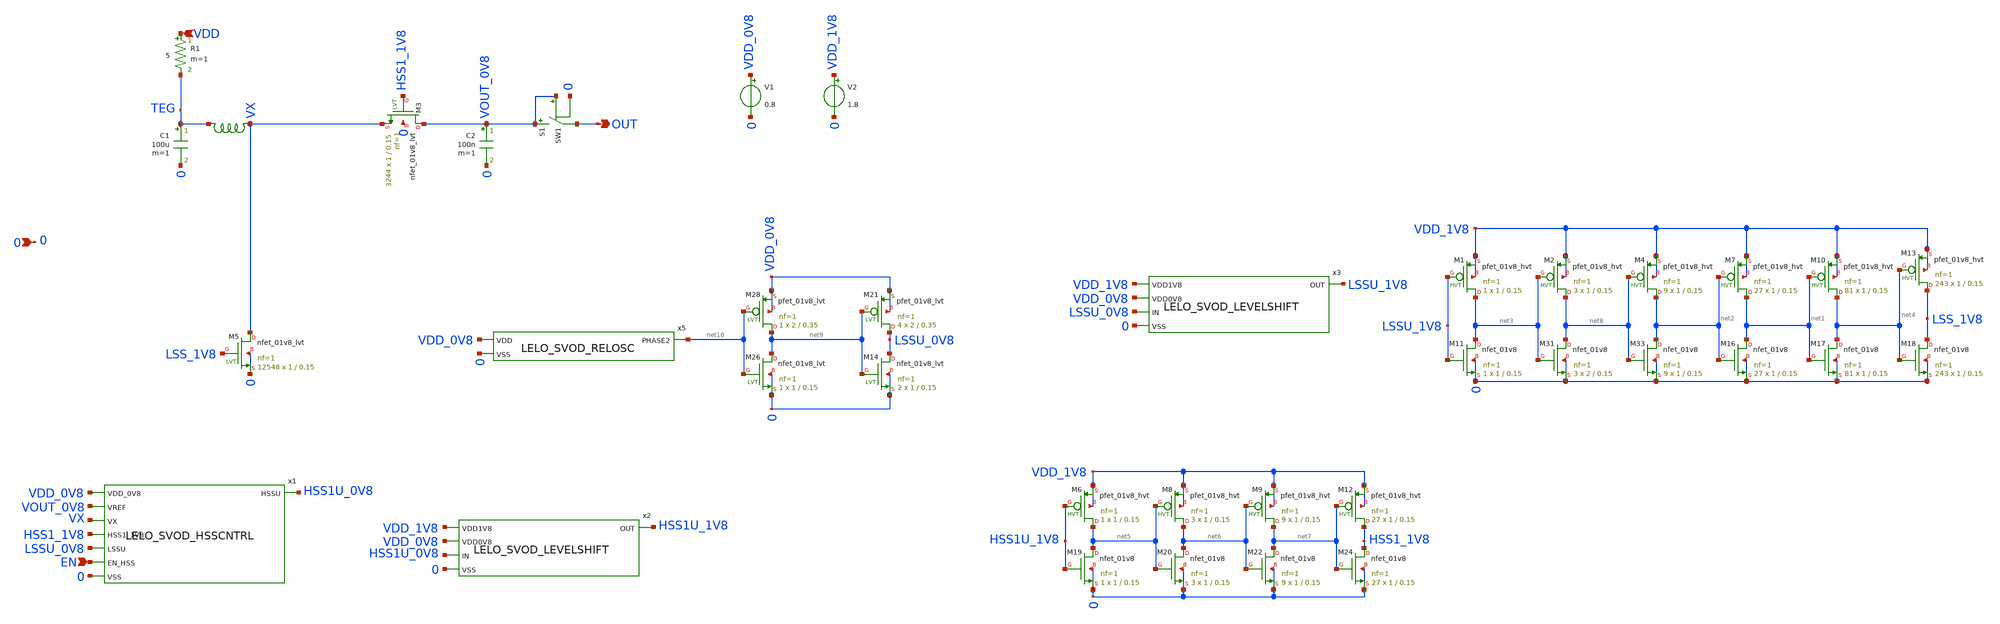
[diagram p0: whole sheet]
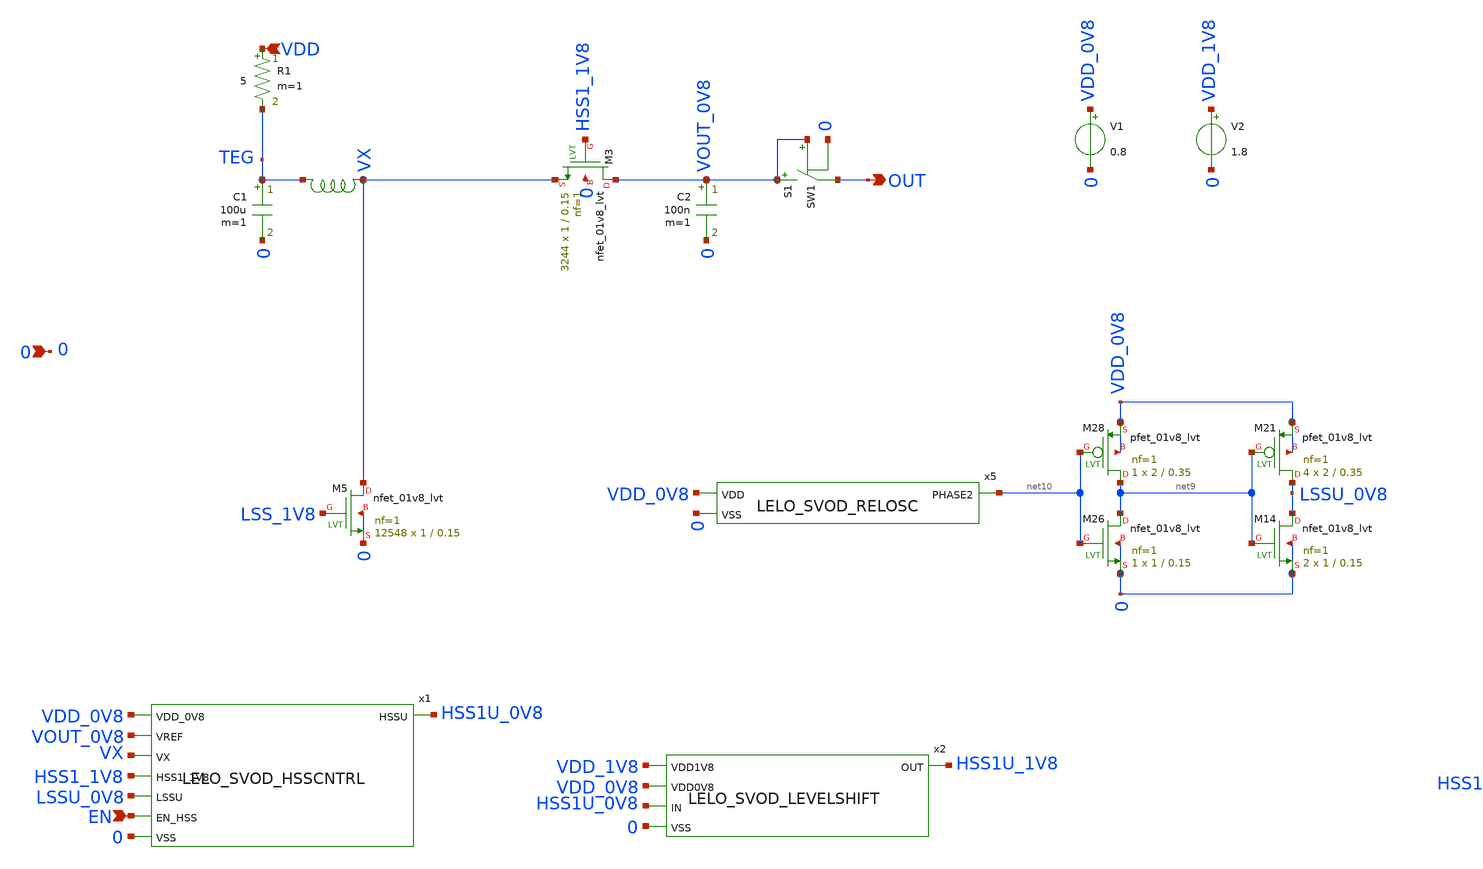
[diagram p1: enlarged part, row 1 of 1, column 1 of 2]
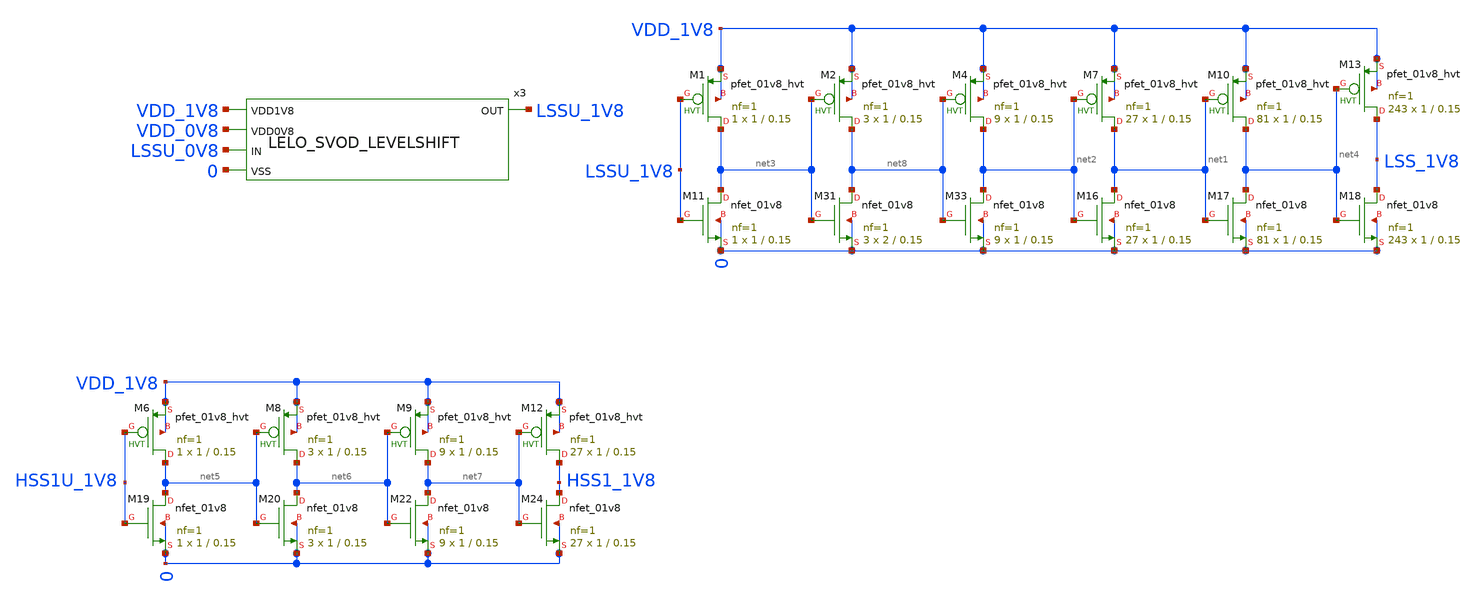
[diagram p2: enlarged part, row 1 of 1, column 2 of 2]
** sch_path: design/LELO_SVOD_SKY130A/LELO_SVOD_0V8_BOOST.sch
**.subckt LELO_SVOD_0V8_BOOST VDD 0 OUT EN
*.ipin VDD
*.ipin 0
*.opin OUT
*.ipin EN
R1 VDD TEG 5 m=1
C1 TEG 0 100u m=1
XM5 VX LSS_1V8 0 0 sky130_fd_pr__nfet_01v8_lvt L=0.15 W=1 nf=1 ad='int((1 + 1)/2) * 1 / 1 * 0.29' as='int((1 + 2)/2) * 1 / 1 * 0.29'
+ pd='2*int((1 + 1)/2) * (1 / 1 + 0.29)' ps='2*int((1 + 2)/2) * (1 / 1 + 0.29)' nrd='0.29 / 1 ' nrs='0.29 / 1 '
+ sa=0 sb=0 sd=0 mult=12548 m=12548
C2 VOUT_0V8 0 100n m=1
XM11 net3 LSSU_1V8 0 0 sky130_fd_pr__nfet_01v8 L=0.15 W=1 nf=1 ad='int((1 + 1)/2) * 1 / 1 * 0.29' as='int((1 + 2)/2) * 1 / 1 * 0.29'
+ pd='2*int((1 + 1)/2) * (1 / 1 + 0.29)' ps='2*int((1 + 2)/2) * (1 / 1 + 0.29)' nrd='0.29 / 1 ' nrs='0.29 / 1 '
+ sa=0 sb=0 sd=0 mult=1 m=1
XM16 net1 net2 0 0 sky130_fd_pr__nfet_01v8 L=0.15 W=1 nf=1 ad='int((1 + 1)/2) * 1 / 1 * 0.29' as='int((1 + 2)/2) * 1 / 1 * 0.29'
+ pd='2*int((1 + 1)/2) * (1 / 1 + 0.29)' ps='2*int((1 + 2)/2) * (1 / 1 + 0.29)' nrd='0.29 / 1 ' nrs='0.29 / 1 '
+ sa=0 sb=0 sd=0 mult=27 m=27
XM17 net4 net1 0 0 sky130_fd_pr__nfet_01v8 L=0.15 W=1 nf=1 ad='int((1 + 1)/2) * 1 / 1 * 0.29' as='int((1 + 2)/2) * 1 / 1 * 0.29'
+ pd='2*int((1 + 1)/2) * (1 / 1 + 0.29)' ps='2*int((1 + 2)/2) * (1 / 1 + 0.29)' nrd='0.29 / 1 ' nrs='0.29 / 1 '
+ sa=0 sb=0 sd=0 mult=81 m=81
XM18 LSS_1V8 net4 0 0 sky130_fd_pr__nfet_01v8 L=0.15 W=1 nf=1 ad='int((1 + 1)/2) * 1 / 1 * 0.29' as='int((1 + 2)/2) * 1 / 1 * 0.29'
+ pd='2*int((1 + 1)/2) * (1 / 1 + 0.29)' ps='2*int((1 + 2)/2) * (1 / 1 + 0.29)' nrd='0.29 / 1 ' nrs='0.29 / 1 '
+ sa=0 sb=0 sd=0 mult=243 m=243
XM19 net5 HSS1U_1V8 0 0 sky130_fd_pr__nfet_01v8 L=0.15 W=1 nf=1 ad='int((1 + 1)/2) * 1 / 1 * 0.29' as='int((1 + 2)/2) * 1 / 1 * 0.29'
+ pd='2*int((1 + 1)/2) * (1 / 1 + 0.29)' ps='2*int((1 + 2)/2) * (1 / 1 + 0.29)' nrd='0.29 / 1 ' nrs='0.29 / 1 '
+ sa=0 sb=0 sd=0 mult=1 m=1
XM20 net6 net5 0 0 sky130_fd_pr__nfet_01v8 L=0.15 W=1 nf=1 ad='int((1 + 1)/2) * 1 / 1 * 0.29' as='int((1 + 2)/2) * 1 / 1 * 0.29'
+ pd='2*int((1 + 1)/2) * (1 / 1 + 0.29)' ps='2*int((1 + 2)/2) * (1 / 1 + 0.29)' nrd='0.29 / 1 ' nrs='0.29 / 1 '
+ sa=0 sb=0 sd=0 mult=3 m=3
XM22 net7 net6 0 0 sky130_fd_pr__nfet_01v8 L=0.15 W=1 nf=1 ad='int((1 + 1)/2) * 1 / 1 * 0.29' as='int((1 + 2)/2) * 1 / 1 * 0.29'
+ pd='2*int((1 + 1)/2) * (1 / 1 + 0.29)' ps='2*int((1 + 2)/2) * (1 / 1 + 0.29)' nrd='0.29 / 1 ' nrs='0.29 / 1 '
+ sa=0 sb=0 sd=0 mult=9 m=9
XM24 HSS1_1V8 net7 0 0 sky130_fd_pr__nfet_01v8 L=0.15 W=1 nf=1 ad='int((1 + 1)/2) * 1 / 1 * 0.29' as='int((1 + 2)/2) * 1 / 1 * 0.29'
+ pd='2*int((1 + 1)/2) * (1 / 1 + 0.29)' ps='2*int((1 + 2)/2) * (1 / 1 + 0.29)' nrd='0.29 / 1 ' nrs='0.29 / 1 '
+ sa=0 sb=0 sd=0 mult=27 m=27
XM31 net8 net3 0 0 sky130_fd_pr__nfet_01v8 L=0.15 W=2 nf=1 ad='int((1 + 1)/2) * 2 / 1 * 0.29' as='int((1 + 2)/2) * 2 / 1 * 0.29'
+ pd='2*int((1 + 1)/2) * (2 / 1 + 0.29)' ps='2*int((1 + 2)/2) * (2 / 1 + 0.29)' nrd='0.29 / 2 ' nrs='0.29 / 2 '
+ sa=0 sb=0 sd=0 mult=3 m=3
XM33 net2 net8 0 0 sky130_fd_pr__nfet_01v8 L=0.15 W=1 nf=1 ad='int((1 + 1)/2) * 1 / 1 * 0.29' as='int((1 + 2)/2) * 1 / 1 * 0.29'
+ pd='2*int((1 + 1)/2) * (1 / 1 + 0.29)' ps='2*int((1 + 2)/2) * (1 / 1 + 0.29)' nrd='0.29 / 1 ' nrs='0.29 / 1 '
+ sa=0 sb=0 sd=0 mult=9 m=9
XM3 VOUT_0V8 HSS1_1V8 VX 0 sky130_fd_pr__nfet_01v8_lvt L=0.15 W=1 nf=1 ad='int((1 + 1)/2) * 1 / 1 * 0.29'
+ as='int((1 + 2)/2) * 1 / 1 * 0.29' pd='2*int((1 + 1)/2) * (1 / 1 + 0.29)' ps='2*int((1 + 2)/2) * (1 / 1 + 0.29)'
+ nrd='0.29 / 1 ' nrs='0.29 / 1 ' sa=0 sb=0 sd=0 mult=3244 m=3244
x1 VDD_0V8 HSS1U_0V8 VOUT_0V8 VX HSS1_1V8 LSSU_0V8 EN 0 LELO_SVOD_HSSCNTRL
x2 VDD_1V8 HSS1U_1V8 VDD_0V8 HSS1U_0V8 0 LELO_SVOD_LEVELSHIFT
x3 VDD_1V8 LSSU_1V8 VDD_0V8 LSSU_0V8 0 LELO_SVOD_LEVELSHIFT
XM6 net5 HSS1U_1V8 VDD_1V8 VDD_1V8 sky130_fd_pr__pfet_01v8_hvt L=0.15 W=1 nf=1 ad='int((1 + 1)/2) * 1 / 1 * 0.29'
+ as='int((1 + 2)/2) * 1 / 1 * 0.29' pd='2*int((1 + 1)/2) * (1 / 1 + 0.29)' ps='2*int((1 + 2)/2) * (1 / 1 + 0.29)'
+ nrd='0.29 / 1 ' nrs='0.29 / 1 ' sa=0 sb=0 sd=0 mult=1 m=1
XM8 net6 net5 VDD_1V8 VDD_1V8 sky130_fd_pr__pfet_01v8_hvt L=0.15 W=1 nf=1 ad='int((1 + 1)/2) * 1 / 1 * 0.29'
+ as='int((1 + 2)/2) * 1 / 1 * 0.29' pd='2*int((1 + 1)/2) * (1 / 1 + 0.29)' ps='2*int((1 + 2)/2) * (1 / 1 + 0.29)'
+ nrd='0.29 / 1 ' nrs='0.29 / 1 ' sa=0 sb=0 sd=0 mult=3 m=3
XM9 net7 net6 VDD_1V8 VDD_1V8 sky130_fd_pr__pfet_01v8_hvt L=0.15 W=1 nf=1 ad='int((1 + 1)/2) * 1 / 1 * 0.29'
+ as='int((1 + 2)/2) * 1 / 1 * 0.29' pd='2*int((1 + 1)/2) * (1 / 1 + 0.29)' ps='2*int((1 + 2)/2) * (1 / 1 + 0.29)'
+ nrd='0.29 / 1 ' nrs='0.29 / 1 ' sa=0 sb=0 sd=0 mult=9 m=9
XM12 HSS1_1V8 net7 VDD_1V8 VDD_1V8 sky130_fd_pr__pfet_01v8_hvt L=0.15 W=1 nf=1 ad='int((1 + 1)/2) * 1 / 1 * 0.29'
+ as='int((1 + 2)/2) * 1 / 1 * 0.29' pd='2*int((1 + 1)/2) * (1 / 1 + 0.29)' ps='2*int((1 + 2)/2) * (1 / 1 + 0.29)'
+ nrd='0.29 / 1 ' nrs='0.29 / 1 ' sa=0 sb=0 sd=0 mult=27 m=27
XM1 net3 LSSU_1V8 VDD_1V8 VDD_1V8 sky130_fd_pr__pfet_01v8_hvt L=0.15 W=1 nf=1 ad='int((1 + 1)/2) * 1 / 1 * 0.29'
+ as='int((1 + 2)/2) * 1 / 1 * 0.29' pd='2*int((1 + 1)/2) * (1 / 1 + 0.29)' ps='2*int((1 + 2)/2) * (1 / 1 + 0.29)'
+ nrd='0.29 / 1 ' nrs='0.29 / 1 ' sa=0 sb=0 sd=0 mult=1 m=1
XM2 net8 net3 VDD_1V8 VDD_1V8 sky130_fd_pr__pfet_01v8_hvt L=0.15 W=1 nf=1 ad='int((1 + 1)/2) * 1 / 1 * 0.29'
+ as='int((1 + 2)/2) * 1 / 1 * 0.29' pd='2*int((1 + 1)/2) * (1 / 1 + 0.29)' ps='2*int((1 + 2)/2) * (1 / 1 + 0.29)'
+ nrd='0.29 / 1 ' nrs='0.29 / 1 ' sa=0 sb=0 sd=0 mult=3 m=3
XM4 net2 net8 VDD_1V8 VDD_1V8 sky130_fd_pr__pfet_01v8_hvt L=0.15 W=1 nf=1 ad='int((1 + 1)/2) * 1 / 1 * 0.29'
+ as='int((1 + 2)/2) * 1 / 1 * 0.29' pd='2*int((1 + 1)/2) * (1 / 1 + 0.29)' ps='2*int((1 + 2)/2) * (1 / 1 + 0.29)'
+ nrd='0.29 / 1 ' nrs='0.29 / 1 ' sa=0 sb=0 sd=0 mult=9 m=9
XM7 net1 net2 VDD_1V8 VDD_1V8 sky130_fd_pr__pfet_01v8_hvt L=0.15 W=1 nf=1 ad='int((1 + 1)/2) * 1 / 1 * 0.29'
+ as='int((1 + 2)/2) * 1 / 1 * 0.29' pd='2*int((1 + 1)/2) * (1 / 1 + 0.29)' ps='2*int((1 + 2)/2) * (1 / 1 + 0.29)'
+ nrd='0.29 / 1 ' nrs='0.29 / 1 ' sa=0 sb=0 sd=0 mult=27 m=27
XM10 net4 net1 VDD_1V8 VDD_1V8 sky130_fd_pr__pfet_01v8_hvt L=0.15 W=1 nf=1 ad='int((1 + 1)/2) * 1 / 1 * 0.29'
+ as='int((1 + 2)/2) * 1 / 1 * 0.29' pd='2*int((1 + 1)/2) * (1 / 1 + 0.29)' ps='2*int((1 + 2)/2) * (1 / 1 + 0.29)'
+ nrd='0.29 / 1 ' nrs='0.29 / 1 ' sa=0 sb=0 sd=0 mult=81 m=81
XM13 LSS_1V8 net4 VDD_1V8 VDD_1V8 sky130_fd_pr__pfet_01v8_hvt L=0.15 W=1 nf=1 ad='int((1 + 1)/2) * 1 / 1 * 0.29'
+ as='int((1 + 2)/2) * 1 / 1 * 0.29' pd='2*int((1 + 1)/2) * (1 / 1 + 0.29)' ps='2*int((1 + 2)/2) * (1 / 1 + 0.29)'
+ nrd='0.29 / 1 ' nrs='0.29 / 1 ' sa=0 sb=0 sd=0 mult=243 m=243
V1 VDD_0V8 0 0.8
V2 VDD_1V8 0 1.8
S1 VOUT_0V8 OUT VOUT_0V8 0 SW1
XM14 LSSU_0V8 net9 0 0 sky130_fd_pr__nfet_01v8_lvt L=0.15 W=1 nf=1 ad='int((1 + 1)/2) * 1 / 1 * 0.29'
+ as='int((1 + 2)/2) * 1 / 1 * 0.29' pd='2*int((1 + 1)/2) * (1 / 1 + 0.29)' ps='2*int((1 + 2)/2) * (1 / 1 + 0.29)'
+ nrd='0.29 / 1 ' nrs='0.29 / 1 ' sa=0 sb=0 sd=0 mult=2 m=2
XM21 LSSU_0V8 net9 VDD_0V8 VDD_0V8 sky130_fd_pr__pfet_01v8_lvt L=0.35 W=2 nf=1 ad='int((1 + 1)/2) * 2 / 1 * 0.29'
+ as='int((1 + 2)/2) * 2 / 1 * 0.29' pd='2*int((1 + 1)/2) * (2 / 1 + 0.29)' ps='2*int((1 + 2)/2) * (2 / 1 + 0.29)'
+ nrd='0.29 / 2 ' nrs='0.29 / 2 ' sa=0 sb=0 sd=0 mult=4 m=4
XM26 net9 net10 0 0 sky130_fd_pr__nfet_01v8_lvt L=0.15 W=1 nf=1 ad='int((1 + 1)/2) * 1 / 1 * 0.29' as='int((1 + 2)/2) * 1 / 1 * 0.29'
+ pd='2*int((1 + 1)/2) * (1 / 1 + 0.29)' ps='2*int((1 + 2)/2) * (1 / 1 + 0.29)' nrd='0.29 / 1 ' nrs='0.29 / 1 '
+ sa=0 sb=0 sd=0 mult=1 m=1
XM28 net9 net10 VDD_0V8 VDD_0V8 sky130_fd_pr__pfet_01v8_lvt L=0.35 W=2 nf=1 ad='int((1 + 1)/2) * 2 / 1 * 0.29'
+ as='int((1 + 2)/2) * 2 / 1 * 0.29' pd='2*int((1 + 1)/2) * (2 / 1 + 0.29)' ps='2*int((1 + 2)/2) * (2 / 1 + 0.29)'
+ nrd='0.29 / 2 ' nrs='0.29 / 2 ' sa=0 sb=0 sd=0 mult=1 m=1
x4 VX TEG XGL6030-183_sat
x5 VDD_0V8 0 net10 LELO_SVOD_RELOSC
**.ends

* expanding   symbol:  LELO_SVOD_SKY130A/LELO_SVOD_HSSCNTRL.sym # of pins=8
** sym_path: design/LELO_SVOD_SKY130A/LELO_SVOD_HSSCNTRL.sym
** sch_path: design/LELO_SVOD_SKY130A/LELO_SVOD_HSSCNTRL.sch
.subckt LELO_SVOD_HSSCNTRL VDD_0V8 HSSU VREF VX HSS1_1V8 LSSU EN_HSS VSS
*.ipin VREF
*.opin HSSU
*.ipin VX
*.ipin LSSU
*.ipin VSS
*.ipin EN_HSS
*.ipin VDD_0V8
*.ipin HSS1_1V8
C7 VX_SAMPL VSS 100f m=1
C3 VOUT_SAMPL VSS 100f m=1
x4 SN SP VDD_0V8 VX_SAMPL VOUT_SAMPL NHSSU HSSUL VSS LELO_CMP
C4 VC VSS 1p m=1
XM9 VC DN net1 VSS sky130_fd_pr__nfet_01v8 L=1 W=0.42 nf=1 ad='int((1 + 1)/2) * 0.42 / 1 * 0.29' as='int((1 + 2)/2) * 0.42 / 1 * 0.29'
+ pd='2*int((1 + 1)/2) * (0.42 / 1 + 0.29)' ps='2*int((1 + 2)/2) * (0.42 / 1 + 0.29)' nrd='0.29 / 0.42 '
+ nrs='0.29 / 0.42 ' sa=0 sb=0 sd=0 mult=1 m=1
x10 VDD_0V8 SP NUP VSS LELO_INV
R5 net1 net3 200k m=1
XM35 net3 CURRENT_ON_N VSS VSS sky130_fd_pr__nfet_01v8 L=1 W=0.42 nf=1 ad='int((1 + 1)/2) * 0.42 / 1 * 0.29'
+ as='int((1 + 2)/2) * 0.42 / 1 * 0.29' pd='2*int((1 + 1)/2) * (0.42 / 1 + 0.29)' ps='2*int((1 + 2)/2) * (0.42 / 1 + 0.29)'
+ nrd='0.29 / 0.42 ' nrs='0.29 / 0.42 ' sa=0 sb=0 sd=0 mult=1 m=1
x11 VDD_0V8 SN net5 VSS LELO_INV
x14 VDD_0V8 net5 DN VSS LELO_INV
x17 VDD_0V8 NUP UP VSS LELO_INV
x2 net9 net6 UP DN VSS LELO_NOR
x3 VDD_0V8 net6 VSS CURRENT_ON_P CURRENT_ON_N LELO_ONESHOT
R3 net4 net2 200k m=1
XM8 VC NUP net2 VDD_0V8 sky130_fd_pr__pfet_01v8_lvt L=1 W=0.42 nf=1 ad='int((1 + 1)/2) * 0.42 / 1 * 0.29'
+ as='int((1 + 2)/2) * 0.42 / 1 * 0.29' pd='2*int((1 + 1)/2) * (0.42 / 1 + 0.29)' ps='2*int((1 + 2)/2) * (0.42 / 1 + 0.29)'
+ nrd='0.29 / 0.42 ' nrs='0.29 / 0.42 ' sa=0 sb=0 sd=0 mult=1 m=1
XM25 net4 CURRENT_ON_P VDD_0V8 VDD_0V8 sky130_fd_pr__pfet_01v8_lvt L=1 W=0.42 nf=1 ad='int((1 + 1)/2) * 0.42 / 1 * 0.29'
+ as='int((1 + 2)/2) * 0.42 / 1 * 0.29' pd='2*int((1 + 1)/2) * (0.42 / 1 + 0.29)' ps='2*int((1 + 2)/2) * (0.42 / 1 + 0.29)'
+ nrd='0.29 / 0.42 ' nrs='0.29 / 0.42 ' sa=0 sb=0 sd=0 mult=1 m=1
x1 VDD_0V8 net8 EN_HSS HSSU VC VSS LELO_ONESHOT_VC
x5 net10 net8 LSSU net7 VSS LELO_NOR
x6 VDD_0V8 EN_HSS net7 VSS LELO_INV
x7 VDD_0V8 HSSU NHSSU VSS LELO_INV
x8 VDD_0V8 NHSSU HSSUL VSS LELO_INV
XM1 VREF HSS1_1V8 VOUT_SAMPL VSS sky130_fd_pr__nfet_01v8 L=0.15 W=1 nf=1 ad='int((1 + 1)/2) * 1 / 1 * 0.29'
+ as='int((1 + 2)/2) * 1 / 1 * 0.29' pd='2*int((1 + 1)/2) * (1 / 1 + 0.29)' ps='2*int((1 + 2)/2) * (1 / 1 + 0.29)'
+ nrd='0.29 / 1 ' nrs='0.29 / 1 ' sa=0 sb=0 sd=0 mult=1 m=1
XM2 VX HSS1_1V8 VX_SAMPL VSS sky130_fd_pr__nfet_01v8 L=0.15 W=1 nf=1 ad='int((1 + 1)/2) * 1 / 1 * 0.29'
+ as='int((1 + 2)/2) * 1 / 1 * 0.29' pd='2*int((1 + 1)/2) * (1 / 1 + 0.29)' ps='2*int((1 + 2)/2) * (1 / 1 + 0.29)'
+ nrd='0.29 / 1 ' nrs='0.29 / 1 ' sa=0 sb=0 sd=0 mult=1 m=1
.ends


* expanding   symbol:  LELO_SVOD_SKY130A/LELO_SVOD_LEVELSHIFT.sym # of pins=5
** sym_path: design/LELO_SVOD_SKY130A/LELO_SVOD_LEVELSHIFT.sym
** sch_path: design/LELO_SVOD_SKY130A/LELO_SVOD_LEVELSHIFT.sch
.subckt LELO_SVOD_LEVELSHIFT VDD1V8 OUT VDD0V8 IN VSS
*.ipin VDD1V8
*.ipin VDD0V8
*.ipin IN
*.ipin VSS
*.opin OUT
XM1 net1 IN VSS VSS sky130_fd_pr__nfet_01v8_lvt L=0.15 W=2 nf=1 ad='int((1 + 1)/2) * 2 / 1 * 0.29' as='int((1 + 2)/2) * 2 / 1 * 0.29'
+ pd='2*int((1 + 1)/2) * (2 / 1 + 0.29)' ps='2*int((1 + 2)/2) * (2 / 1 + 0.29)' nrd='0.29 / 2 ' nrs='0.29 / 2 '
+ sa=0 sb=0 sd=0 mult=1 m=1
XM2 OUT net2 VSS VSS sky130_fd_pr__nfet_01v8_lvt L=0.15 W=2 nf=1 ad='int((1 + 1)/2) * 2 / 1 * 0.29' as='int((1 + 2)/2) * 2 / 1 * 0.29'
+ pd='2*int((1 + 1)/2) * (2 / 1 + 0.29)' ps='2*int((1 + 2)/2) * (2 / 1 + 0.29)' nrd='0.29 / 2 ' nrs='0.29 / 2 '
+ sa=0 sb=0 sd=0 mult=1 m=1
x1 VDD0V8 IN net2 VSS LELO_INV
XM3 net1 OUT VDD1V8 VDD1V8 sky130_fd_pr__pfet_01v8 L=0.15 W=1 nf=1 ad='int((1 + 1)/2) * 1 / 1 * 0.29'
+ as='int((1 + 2)/2) * 1 / 1 * 0.29' pd='2*int((1 + 1)/2) * (1 / 1 + 0.29)' ps='2*int((1 + 2)/2) * (1 / 1 + 0.29)'
+ nrd='0.29 / 1 ' nrs='0.29 / 1 ' sa=0 sb=0 sd=0 mult=1 m=1
XM4 OUT net1 VDD1V8 VDD1V8 sky130_fd_pr__pfet_01v8 L=0.15 W=1 nf=1 ad='int((1 + 1)/2) * 1 / 1 * 0.29'
+ as='int((1 + 2)/2) * 1 / 1 * 0.29' pd='2*int((1 + 1)/2) * (1 / 1 + 0.29)' ps='2*int((1 + 2)/2) * (1 / 1 + 0.29)'
+ nrd='0.29 / 1 ' nrs='0.29 / 1 ' sa=0 sb=0 sd=0 mult=1 m=1
.ends


* expanding   symbol:  LELO_SVOD_SKY130A/XGL6030-183_sat.sym # of pins=2
** sym_path: design/LELO_SVOD_SKY130A/XGL6030-183_sat.sym

.subckt XGL6030-183_sat port1 port2
X1 port1 port2 Model1C R1=5 R2=0.08 C= 14.5p K1=0.000001 K2=3.86 K3= 18u K4=0.000001 K5=0.000001
+ L=1.6855E-05 Is=9.6842 a=0.6947 L_Z0=0 L_EL=0 L_F0=0E6 PkZ=11551.4391
.ends XGL6030-183_sat


* expanding   symbol:  LELO_SVOD_SKY130A/LELO_SVOD_RELOSC.sym # of pins=3
** sym_path: design/LELO_SVOD_SKY130A/LELO_SVOD_RELOSC.sym
** sch_path: design/LELO_SVOD_SKY130A/LELO_SVOD_RELOSC.sch
.subckt LELO_SVOD_RELOSC VDD VSS PHASE2
*.ipin VDD
*.ipin VSS
*.opin PHASE2
XM1 BIAS BIAS net2 net2 sky130_fd_pr__nfet_01v8_lvt L=0.15 W=1 nf=1 ad='int((1 + 1)/2) * 1 / 1 * 0.29'
+ as='int((1 + 2)/2) * 1 / 1 * 0.29' pd='2*int((1 + 1)/2) * (1 / 1 + 0.29)' ps='2*int((1 + 2)/2) * (1 / 1 + 0.29)'
+ nrd='0.29 / 1 ' nrs='0.29 / 1 ' sa=0 sb=0 sd=0 mult=1 m=1
XM2 net7 BIAS net1 net1 sky130_fd_pr__nfet_01v8_lvt L=0.15 W=1 nf=1 ad='int((1 + 1)/2) * 1 / 1 * 0.29'
+ as='int((1 + 2)/2) * 1 / 1 * 0.29' pd='2*int((1 + 1)/2) * (1 / 1 + 0.29)' ps='2*int((1 + 2)/2) * (1 / 1 + 0.29)'
+ nrd='0.29 / 1 ' nrs='0.29 / 1 ' sa=0 sb=0 sd=0 mult=1 m=1
XM3 net6 BIAS net3 net3 sky130_fd_pr__nfet_01v8_lvt L=0.15 W=1 nf=1 ad='int((1 + 1)/2) * 1 / 1 * 0.29'
+ as='int((1 + 2)/2) * 1 / 1 * 0.29' pd='2*int((1 + 1)/2) * (1 / 1 + 0.29)' ps='2*int((1 + 2)/2) * (1 / 1 + 0.29)'
+ nrd='0.29 / 1 ' nrs='0.29 / 1 ' sa=0 sb=0 sd=0 mult=1 m=1
R1 net2 VSS 10000000 m=1
C1 net1 VSS 1.71p m=1
C2 net3 VSS 1.9p m=1
XM4 net1 PHASE2 VSS VSS sky130_fd_pr__nfet_01v8_lvt L=0.15 W=1 nf=1 ad='int((1 + 1)/2) * 1 / 1 * 0.29'
+ as='int((1 + 2)/2) * 1 / 1 * 0.29' pd='2*int((1 + 1)/2) * (1 / 1 + 0.29)' ps='2*int((1 + 2)/2) * (1 / 1 + 0.29)'
+ nrd='0.29 / 1 ' nrs='0.29 / 1 ' sa=0 sb=0 sd=0 mult=10 m=10
XM5 net3 PHASE1 VSS VSS sky130_fd_pr__nfet_01v8_lvt L=0.15 W=1 nf=1 ad='int((1 + 1)/2) * 1 / 1 * 0.29'
+ as='int((1 + 2)/2) * 1 / 1 * 0.29' pd='2*int((1 + 1)/2) * (1 / 1 + 0.29)' ps='2*int((1 + 2)/2) * (1 / 1 + 0.29)'
+ nrd='0.29 / 1 ' nrs='0.29 / 1 ' sa=0 sb=0 sd=0 mult=10 m=10
x1 net10 net5 net6 net4 VSS LELO_NOR
x2 net11 net4 net5 net7 VSS LELO_NOR
XM6 net7 PHASE2 net8 net8 sky130_fd_pr__pfet_01v8_lvt L=0.35 W=1 nf=1 ad='int((1 + 1)/2) * 1 / 1 * 0.29'
+ as='int((1 + 2)/2) * 1 / 1 * 0.29' pd='2*int((1 + 1)/2) * (1 / 1 + 0.29)' ps='2*int((1 + 2)/2) * (1 / 1 + 0.29)'
+ nrd='0.29 / 1 ' nrs='0.29 / 1 ' sa=0 sb=0 sd=0 mult=1 m=1
XM7 net6 PHASE1 net8 net8 sky130_fd_pr__pfet_01v8_lvt L=0.35 W=1 nf=1 ad='int((1 + 1)/2) * 1 / 1 * 0.29'
+ as='int((1 + 2)/2) * 1 / 1 * 0.29' pd='2*int((1 + 1)/2) * (1 / 1 + 0.29)' ps='2*int((1 + 2)/2) * (1 / 1 + 0.29)'
+ nrd='0.29 / 1 ' nrs='0.29 / 1 ' sa=0 sb=0 sd=0 mult=1 m=1
x3 VDD net5 PHASE1 VSS LELO_INV
x4 VDD net4 PHASE2 VSS LELO_INV
I2 net9 VSS 10n
XM8 net9 net9 VDD VDD sky130_fd_pr__pfet_01v8_lvt L=0.35 W=1 nf=1 ad='int((1 + 1)/2) * 1 / 1 * 0.29'
+ as='int((1 + 2)/2) * 1 / 1 * 0.29' pd='2*int((1 + 1)/2) * (1 / 1 + 0.29)' ps='2*int((1 + 2)/2) * (1 / 1 + 0.29)'
+ nrd='0.29 / 1 ' nrs='0.29 / 1 ' sa=0 sb=0 sd=0 mult=1 m=1
XM9 BIAS net9 VDD VDD sky130_fd_pr__pfet_01v8_lvt L=0.35 W=1 nf=1 ad='int((1 + 1)/2) * 1 / 1 * 0.29'
+ as='int((1 + 2)/2) * 1 / 1 * 0.29' pd='2*int((1 + 1)/2) * (1 / 1 + 0.29)' ps='2*int((1 + 2)/2) * (1 / 1 + 0.29)'
+ nrd='0.29 / 1 ' nrs='0.29 / 1 ' sa=0 sb=0 sd=0 mult=1 m=1
XM10 net8 net9 VDD VDD sky130_fd_pr__pfet_01v8_lvt L=0.35 W=1 nf=1 ad='int((1 + 1)/2) * 1 / 1 * 0.29'
+ as='int((1 + 2)/2) * 1 / 1 * 0.29' pd='2*int((1 + 1)/2) * (1 / 1 + 0.29)' ps='2*int((1 + 2)/2) * (1 / 1 + 0.29)'
+ nrd='0.29 / 1 ' nrs='0.29 / 1 ' sa=0 sb=0 sd=0 mult=1 m=1
.ends


* expanding   symbol:  LELO_SVOD_SKY130A/LELO_CMP.sym # of pins=8
** sym_path: design/LELO_SVOD_SKY130A/LELO_CMP.sym
** sch_path: design/LELO_SVOD_SKY130A/LELO_CMP.sch
.subckt LELO_CMP SN SP VDD VIP VIN CLK CLKN VSS
*.ipin VIP
*.ipin VIN
*.ipin CLK
*.ipin CLKN
*.ipin VDD
*.ipin VSS
*.opin SN
*.opin SP
XM2 SN net3 net5 VDD sky130_fd_pr__pfet_01v8_lvt L=0.44 W=1.92 nf=2 ad='int((2 + 1)/2) * 1.92 / 2 * 0.29'
+ as='int((2 + 2)/2) * 1.92 / 2 * 0.29' pd='2*int((2 + 1)/2) * (1.92 / 2 + 0.29)' ps='2*int((2 + 2)/2) * (1.92 / 2 + 0.29)'
+ nrd='0.29 / 1.92 ' nrs='0.29 / 1.92 ' sa=0 sb=0 sd=0 mult=3 m=3
XM1 SP net2 net6 VDD sky130_fd_pr__pfet_01v8_lvt L=0.44 W=1.92 nf=2 ad='int((2 + 1)/2) * 1.92 / 2 * 0.29'
+ as='int((2 + 2)/2) * 1.92 / 2 * 0.29' pd='2*int((2 + 1)/2) * (1.92 / 2 + 0.29)' ps='2*int((2 + 2)/2) * (1.92 / 2 + 0.29)'
+ nrd='0.29 / 1.92 ' nrs='0.29 / 1.92 ' sa=0 sb=0 sd=0 mult=3 m=3
XM3 net2 VIP net1 VSS sky130_fd_pr__nfet_01v8_lvt L=0.44 W=6.4 nf=1 ad='int((1 + 1)/2) * 6.4 / 1 * 0.29'
+ as='int((1 + 2)/2) * 6.4 / 1 * 0.29' pd='2*int((1 + 1)/2) * (6.4 / 1 + 0.29)' ps='2*int((1 + 2)/2) * (6.4 / 1 + 0.29)'
+ nrd='0.29 / 6.4 ' nrs='0.29 / 6.4 ' sa=0 sb=0 sd=0 mult=1 m=1
XM4 net3 VIN net1 VSS sky130_fd_pr__nfet_01v8_lvt L=0.44 W=6.4 nf=1 ad='int((1 + 1)/2) * 6.4 / 1 * 0.29'
+ as='int((1 + 2)/2) * 6.4 / 1 * 0.29' pd='2*int((1 + 1)/2) * (6.4 / 1 + 0.29)' ps='2*int((1 + 2)/2) * (6.4 / 1 + 0.29)'
+ nrd='0.29 / 6.4 ' nrs='0.29 / 6.4 ' sa=0 sb=0 sd=0 mult=1 m=1
XM5 net3 CLK VDD VDD sky130_fd_pr__pfet_01v8_lvt L=0.94 W=1.92 nf=2 ad='int((2 + 1)/2) * 1.92 / 2 * 0.29'
+ as='int((2 + 2)/2) * 1.92 / 2 * 0.29' pd='2*int((2 + 1)/2) * (1.92 / 2 + 0.29)' ps='2*int((2 + 2)/2) * (1.92 / 2 + 0.29)'
+ nrd='0.29 / 1.92 ' nrs='0.29 / 1.92 ' sa=0 sb=0 sd=0 mult=1 m=1
XM6 net6 SN VDD VDD sky130_fd_pr__pfet_01v8_lvt L=0.94 W=1.92 nf=2 ad='int((2 + 1)/2) * 1.92 / 2 * 0.29'
+ as='int((2 + 2)/2) * 1.92 / 2 * 0.29' pd='2*int((2 + 1)/2) * (1.92 / 2 + 0.29)' ps='2*int((2 + 2)/2) * (1.92 / 2 + 0.29)'
+ nrd='0.29 / 1.92 ' nrs='0.29 / 1.92 ' sa=0 sb=0 sd=0 mult=1 m=1
XM7 net5 SP VDD VDD sky130_fd_pr__pfet_01v8_lvt L=0.94 W=1.92 nf=2 ad='int((2 + 1)/2) * 1.92 / 2 * 0.29'
+ as='int((2 + 2)/2) * 1.92 / 2 * 0.29' pd='2*int((2 + 1)/2) * (1.92 / 2 + 0.29)' ps='2*int((2 + 2)/2) * (1.92 / 2 + 0.29)'
+ nrd='0.29 / 1.92 ' nrs='0.29 / 1.92 ' sa=0 sb=0 sd=0 mult=1 m=1
XM8 net2 CLK VDD VDD sky130_fd_pr__pfet_01v8_lvt L=0.94 W=1.92 nf=2 ad='int((2 + 1)/2) * 1.92 / 2 * 0.29'
+ as='int((2 + 2)/2) * 1.92 / 2 * 0.29' pd='2*int((2 + 1)/2) * (1.92 / 2 + 0.29)' ps='2*int((2 + 2)/2) * (1.92 / 2 + 0.29)'
+ nrd='0.29 / 1.92 ' nrs='0.29 / 1.92 ' sa=0 sb=0 sd=0 mult=1 m=1
XM9 net1 CLK net4 VSS sky130_fd_pr__nfet_01v8 L=0.94 W=1.92 nf=2 ad='int((2 + 1)/2) * 1.92 / 2 * 0.29'
+ as='int((2 + 2)/2) * 1.92 / 2 * 0.29' pd='2*int((2 + 1)/2) * (1.92 / 2 + 0.29)' ps='2*int((2 + 2)/2) * (1.92 / 2 + 0.29)'
+ nrd='0.29 / 1.92 ' nrs='0.29 / 1.92 ' sa=0 sb=0 sd=0 mult=1 m=1
XM10 net4 CLK VSS VSS sky130_fd_pr__nfet_01v8 L=0.94 W=1.92 nf=2 ad='int((2 + 1)/2) * 1.92 / 2 * 0.29'
+ as='int((2 + 2)/2) * 1.92 / 2 * 0.29' pd='2*int((2 + 1)/2) * (1.92 / 2 + 0.29)' ps='2*int((2 + 2)/2) * (1.92 / 2 + 0.29)'
+ nrd='0.29 / 1.92 ' nrs='0.29 / 1.92 ' sa=0 sb=0 sd=0 mult=1 m=1
XM11 SN CLKN VSS VSS sky130_fd_pr__nfet_01v8 L=0.94 W=1.92 nf=2 ad='int((2 + 1)/2) * 1.92 / 2 * 0.29'
+ as='int((2 + 2)/2) * 1.92 / 2 * 0.29' pd='2*int((2 + 1)/2) * (1.92 / 2 + 0.29)' ps='2*int((2 + 2)/2) * (1.92 / 2 + 0.29)'
+ nrd='0.29 / 1.92 ' nrs='0.29 / 1.92 ' sa=0 sb=0 sd=0 mult=1 m=1
XM12 SP SN VSS VSS sky130_fd_pr__nfet_01v8 L=0.94 W=1.92 nf=2 ad='int((2 + 1)/2) * 1.92 / 2 * 0.29' as='int((2 + 2)/2) * 1.92 / 2 * 0.29'
+ pd='2*int((2 + 1)/2) * (1.92 / 2 + 0.29)' ps='2*int((2 + 2)/2) * (1.92 / 2 + 0.29)' nrd='0.29 / 1.92 '
+ nrs='0.29 / 1.92 ' sa=0 sb=0 sd=0 mult=1 m=1
XM13 SN SP VSS VSS sky130_fd_pr__nfet_01v8 L=0.94 W=1.92 nf=2 ad='int((2 + 1)/2) * 1.92 / 2 * 0.29' as='int((2 + 2)/2) * 1.92 / 2 * 0.29'
+ pd='2*int((2 + 1)/2) * (1.92 / 2 + 0.29)' ps='2*int((2 + 2)/2) * (1.92 / 2 + 0.29)' nrd='0.29 / 1.92 '
+ nrs='0.29 / 1.92 ' sa=0 sb=0 sd=0 mult=1 m=1
XM14 SP CLKN VSS VSS sky130_fd_pr__nfet_01v8 L=0.94 W=1.92 nf=2 ad='int((2 + 1)/2) * 1.92 / 2 * 0.29'
+ as='int((2 + 2)/2) * 1.92 / 2 * 0.29' pd='2*int((2 + 1)/2) * (1.92 / 2 + 0.29)' ps='2*int((2 + 2)/2) * (1.92 / 2 + 0.29)'
+ nrd='0.29 / 1.92 ' nrs='0.29 / 1.92 ' sa=0 sb=0 sd=0 mult=1 m=1
.ends


* expanding   symbol:  LELO_SVOD_SKY130A/LELO_INV.sym # of pins=4
** sym_path: design/LELO_SVOD_SKY130A/LELO_INV.sym
** sch_path: design/LELO_SVOD_SKY130A/LELO_INV.sch
.subckt LELO_INV VDD VIN VOUT GND
*.ipin VIN
*.ipin VDD
*.ipin GND
*.opin VOUT
XM1 VOUT VIN GND GND sky130_fd_pr__nfet_01v8_lvt L=0.15 W=1 nf=1 ad='int((1 + 1)/2) * 1 / 1 * 0.29' as='int((1 + 2)/2) * 1 / 1 * 0.29'
+ pd='2*int((1 + 1)/2) * (1 / 1 + 0.29)' ps='2*int((1 + 2)/2) * (1 / 1 + 0.29)' nrd='0.29 / 1 ' nrs='0.29 / 1 '
+ sa=0 sb=0 sd=0 mult=1 m=1
XM2 VOUT VIN VDD VDD sky130_fd_pr__pfet_01v8_lvt L=0.35 W=1 nf=1 ad='int((1 + 1)/2) * 1 / 1 * 0.29' as='int((1 + 2)/2) * 1 / 1 * 0.29'
+ pd='2*int((1 + 1)/2) * (1 / 1 + 0.29)' ps='2*int((1 + 2)/2) * (1 / 1 + 0.29)' nrd='0.29 / 1 ' nrs='0.29 / 1 '
+ sa=0 sb=0 sd=0 mult=2 m=2
.ends


* expanding   symbol:  LELO_SVOD_SKY130A/LELO_NOR.sym # of pins=5
** sym_path: design/LELO_SVOD_SKY130A/LELO_NOR.sym
** sch_path: design/LELO_SVOD_SKY130A/LELO_NOR.sch
.subckt LELO_NOR VDD OUT A B VSS
*.ipin VDD
*.ipin VSS
*.opin OUT
*.ipin A
*.ipin B
XM2 OUT B VSS VSS sky130_fd_pr__nfet_01v8 L=0.15 W=2 nf=1 ad='int((1 + 1)/2) * 2 / 1 * 0.29' as='int((1 + 2)/2) * 2 / 1 * 0.29'
+ pd='2*int((1 + 1)/2) * (2 / 1 + 0.29)' ps='2*int((1 + 2)/2) * (2 / 1 + 0.29)' nrd='0.29 / 2 ' nrs='0.29 / 2 '
+ sa=0 sb=0 sd=0 mult=1 m=1
XM1 OUT A VSS VSS sky130_fd_pr__nfet_01v8 L=0.15 W=2 nf=1 ad='int((1 + 1)/2) * 2 / 1 * 0.29' as='int((1 + 2)/2) * 2 / 1 * 0.29'
+ pd='2*int((1 + 1)/2) * (2 / 1 + 0.29)' ps='2*int((1 + 2)/2) * (2 / 1 + 0.29)' nrd='0.29 / 2 ' nrs='0.29 / 2 '
+ sa=0 sb=0 sd=0 mult=1 m=1
XM3 OUT B net1 VDD sky130_fd_pr__pfet_01v8 L=0.15 W=4 nf=1 ad='int((1 + 1)/2) * 4 / 1 * 0.29' as='int((1 + 2)/2) * 4 / 1 * 0.29'
+ pd='2*int((1 + 1)/2) * (4 / 1 + 0.29)' ps='2*int((1 + 2)/2) * (4 / 1 + 0.29)' nrd='0.29 / 4 ' nrs='0.29 / 4 '
+ sa=0 sb=0 sd=0 mult=1 m=1
XM4 net1 A VDD VDD sky130_fd_pr__pfet_01v8 L=0.15 W=4 nf=1 ad='int((1 + 1)/2) * 4 / 1 * 0.29' as='int((1 + 2)/2) * 4 / 1 * 0.29'
+ pd='2*int((1 + 1)/2) * (4 / 1 + 0.29)' ps='2*int((1 + 2)/2) * (4 / 1 + 0.29)' nrd='0.29 / 4 ' nrs='0.29 / 4 '
+ sa=0 sb=0 sd=0 mult=1 m=1
.ends


* expanding   symbol:  LELO_SVOD_SKY130A/LELO_ONESHOT.sym # of pins=5
** sym_path: design/LELO_SVOD_SKY130A/LELO_ONESHOT.sym
** sch_path: design/LELO_SVOD_SKY130A/LELO_ONESHOT.sch
.subckt LELO_ONESHOT VDD IN VSS PULSEN PULSE
*.ipin VDD
*.ipin IN
*.ipin VSS
*.opin PULSEN
*.opin PULSE
x8 VDD PULSE PULSEN VSS LELO_INV
x12 VDD net3 net1 PULSE VSS LELO_NOR
C6 net2 net3 100f m=1
x13 VDD net2 PULSE VSS LELO_INV
x18 VDD IN net1 VSS LELO_INV
XM1 net2 0 VDD VDD sky130_fd_pr__pfet_01v8_lvt L=1 W=0.42 nf=1 ad='int((1 + 1)/2) * 0.42 / 1 * 0.29'
+ as='int((1 + 2)/2) * 0.42 / 1 * 0.29' pd='2*int((1 + 1)/2) * (0.42 / 1 + 0.29)' ps='2*int((1 + 2)/2) * (0.42 / 1 + 0.29)'
+ nrd='0.29 / 0.42 ' nrs='0.29 / 0.42 ' sa=0 sb=0 sd=0 mult=1 m=1
.ends


* expanding   symbol:  LELO_SVOD_SKY130A/LELO_ONESHOT_VC.sym # of pins=6
** sym_path: design/LELO_SVOD_SKY130A/LELO_ONESHOT_VC.sym
** sch_path: design/LELO_SVOD_SKY130A/LELO_ONESHOT_VC.sch
.subckt LELO_ONESHOT_VC VDD IN EN OUT VC VSS
*.ipin VDD
*.ipin IN
*.ipin VC
*.ipin VSS
*.opin OUT
*.ipin EN
x2 net3 net2 IN OUT VSS LELO_NOR
C5 net1 net2 20f m=1
x3 VDD net1 OUT VSS LELO_INV
XM4 net1 VC VDD VDD sky130_fd_pr__pfet_01v8_lvt L=10 W=0.42 nf=1 ad='int((1 + 1)/2) * 0.42 / 1 * 0.29'
+ as='int((1 + 2)/2) * 0.42 / 1 * 0.29' pd='2*int((1 + 1)/2) * (0.42 / 1 + 0.29)' ps='2*int((1 + 2)/2) * (0.42 / 1 + 0.29)'
+ nrd='0.29 / 0.42 ' nrs='0.29 / 0.42 ' sa=0 sb=0 sd=0 mult=1 m=1
XM1 net1 VSS VDD VDD sky130_fd_pr__pfet_01v8 L=1 W=0.42 nf=1 ad='int((1 + 1)/2) * 0.42 / 1 * 0.29' as='int((1 + 2)/2) * 0.42 / 1 * 0.29'
+ pd='2*int((1 + 1)/2) * (0.42 / 1 + 0.29)' ps='2*int((1 + 2)/2) * (0.42 / 1 + 0.29)' nrd='0.29 / 0.42 '
+ nrs='0.29 / 0.42 ' sa=0 sb=0 sd=0 mult=1 m=1
XM2 net1 EN VDD VDD sky130_fd_pr__pfet_01v8 L=0.15 W=1 nf=1 ad='int((1 + 1)/2) * 1 / 1 * 0.29' as='int((1 + 2)/2) * 1 / 1 * 0.29'
+ pd='2*int((1 + 1)/2) * (1 / 1 + 0.29)' ps='2*int((1 + 2)/2) * (1 / 1 + 0.29)' nrd='0.29 / 1 ' nrs='0.29 / 1 '
+ sa=0 sb=0 sd=0 mult=10 m=10
.ends

**** begin user architecture code
.MODEL SW1 SW   VT=0.8 VH=0.001  RON=0.001 ROFF=10G
**** end user architecture code
.end
